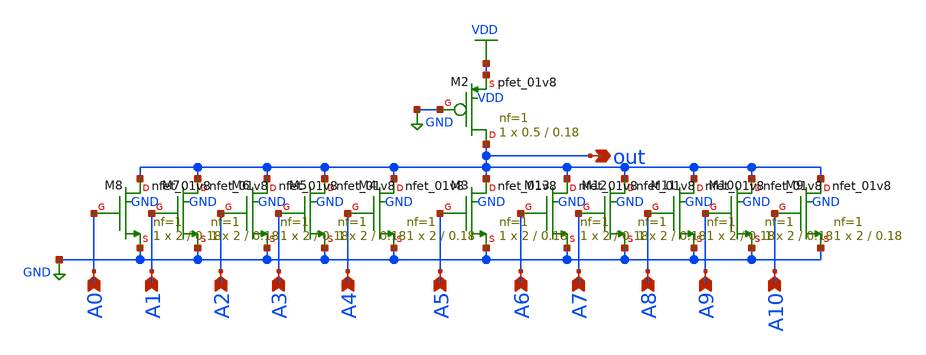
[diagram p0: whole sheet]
** sch_path: xschem/sparse_nor/sparse_nor.sch
**.subckt sparse_nor out A0 A1 A2 A3 A4 A5 A6 A7 A8 A9 A10
*.opin out
*.ipin A0
*.ipin A1
*.ipin A2
*.ipin A3
*.ipin A4
*.ipin A5
*.ipin A6
*.ipin A7
*.ipin A8
*.ipin A9
*.ipin A10
XM2 out GND VDD VDD sky130_fd_pr__pfet_01v8 L=0.18 W=0.5 nf=1 ad='int((nf+1)/2) * W/nf * 0.29' as='int((nf+2)/2) * W/nf * 0.29'
+ pd='2*int((nf+1)/2) * (W/nf + 0.29)' ps='2*int((nf+2)/2) * (W/nf + 0.29)' nrd='0.29 / W' nrs='0.29 / W'
+ sa=0 sb=0 sd=0 mult=1 m=1
XM3 out A5 GND GND sky130_fd_pr__nfet_01v8 L=0.18 W=2 nf=1 ad='int((nf+1)/2) * W/nf * 0.29' as='int((nf+2)/2) * W/nf * 0.29'
+ pd='2*int((nf+1)/2) * (W/nf + 0.29)' ps='2*int((nf+2)/2) * (W/nf + 0.29)' nrd='0.29 / W' nrs='0.29 / W'
+ sa=0 sb=0 sd=0 mult=1 m=1
XM4 out A4 GND GND sky130_fd_pr__nfet_01v8 L=0.18 W=2 nf=1 ad='int((nf+1)/2) * W/nf * 0.29' as='int((nf+2)/2) * W/nf * 0.29'
+ pd='2*int((nf+1)/2) * (W/nf + 0.29)' ps='2*int((nf+2)/2) * (W/nf + 0.29)' nrd='0.29 / W' nrs='0.29 / W'
+ sa=0 sb=0 sd=0 mult=1 m=1
XM5 out A3 GND GND sky130_fd_pr__nfet_01v8 L=0.18 W=2 nf=1 ad='int((nf+1)/2) * W/nf * 0.29' as='int((nf+2)/2) * W/nf * 0.29'
+ pd='2*int((nf+1)/2) * (W/nf + 0.29)' ps='2*int((nf+2)/2) * (W/nf + 0.29)' nrd='0.29 / W' nrs='0.29 / W'
+ sa=0 sb=0 sd=0 mult=1 m=1
XM6 out A2 GND GND sky130_fd_pr__nfet_01v8 L=0.18 W=2 nf=1 ad='int((nf+1)/2) * W/nf * 0.29' as='int((nf+2)/2) * W/nf * 0.29'
+ pd='2*int((nf+1)/2) * (W/nf + 0.29)' ps='2*int((nf+2)/2) * (W/nf + 0.29)' nrd='0.29 / W' nrs='0.29 / W'
+ sa=0 sb=0 sd=0 mult=1 m=1
XM7 out A1 GND GND sky130_fd_pr__nfet_01v8 L=0.18 W=2 nf=1 ad='int((nf+1)/2) * W/nf * 0.29' as='int((nf+2)/2) * W/nf * 0.29'
+ pd='2*int((nf+1)/2) * (W/nf + 0.29)' ps='2*int((nf+2)/2) * (W/nf + 0.29)' nrd='0.29 / W' nrs='0.29 / W'
+ sa=0 sb=0 sd=0 mult=1 m=1
XM8 out A0 GND GND sky130_fd_pr__nfet_01v8 L=0.18 W=2 nf=1 ad='int((nf+1)/2) * W/nf * 0.29' as='int((nf+2)/2) * W/nf * 0.29'
+ pd='2*int((nf+1)/2) * (W/nf + 0.29)' ps='2*int((nf+2)/2) * (W/nf + 0.29)' nrd='0.29 / W' nrs='0.29 / W'
+ sa=0 sb=0 sd=0 mult=1 m=1
XM9 out A10 GND GND sky130_fd_pr__nfet_01v8 L=0.18 W=2 nf=1 ad='int((nf+1)/2) * W/nf * 0.29' as='int((nf+2)/2) * W/nf * 0.29'
+ pd='2*int((nf+1)/2) * (W/nf + 0.29)' ps='2*int((nf+2)/2) * (W/nf + 0.29)' nrd='0.29 / W' nrs='0.29 / W'
+ sa=0 sb=0 sd=0 mult=1 m=1
XM10 out A9 GND GND sky130_fd_pr__nfet_01v8 L=0.18 W=2 nf=1 ad='int((nf+1)/2) * W/nf * 0.29' as='int((nf+2)/2) * W/nf * 0.29'
+ pd='2*int((nf+1)/2) * (W/nf + 0.29)' ps='2*int((nf+2)/2) * (W/nf + 0.29)' nrd='0.29 / W' nrs='0.29 / W'
+ sa=0 sb=0 sd=0 mult=1 m=1
XM11 out A8 GND GND sky130_fd_pr__nfet_01v8 L=0.18 W=2 nf=1 ad='int((nf+1)/2) * W/nf * 0.29' as='int((nf+2)/2) * W/nf * 0.29'
+ pd='2*int((nf+1)/2) * (W/nf + 0.29)' ps='2*int((nf+2)/2) * (W/nf + 0.29)' nrd='0.29 / W' nrs='0.29 / W'
+ sa=0 sb=0 sd=0 mult=1 m=1
XM12 out A7 GND GND sky130_fd_pr__nfet_01v8 L=0.18 W=2 nf=1 ad='int((nf+1)/2) * W/nf * 0.29' as='int((nf+2)/2) * W/nf * 0.29'
+ pd='2*int((nf+1)/2) * (W/nf + 0.29)' ps='2*int((nf+2)/2) * (W/nf + 0.29)' nrd='0.29 / W' nrs='0.29 / W'
+ sa=0 sb=0 sd=0 mult=1 m=1
XM13 out A6 GND GND sky130_fd_pr__nfet_01v8 L=0.18 W=2 nf=1 ad='int((nf+1)/2) * W/nf * 0.29' as='int((nf+2)/2) * W/nf * 0.29'
+ pd='2*int((nf+1)/2) * (W/nf + 0.29)' ps='2*int((nf+2)/2) * (W/nf + 0.29)' nrd='0.29 / W' nrs='0.29 / W'
+ sa=0 sb=0 sd=0 mult=1 m=1
**.ends
.GLOBAL VDD
.GLOBAL GND
.end
